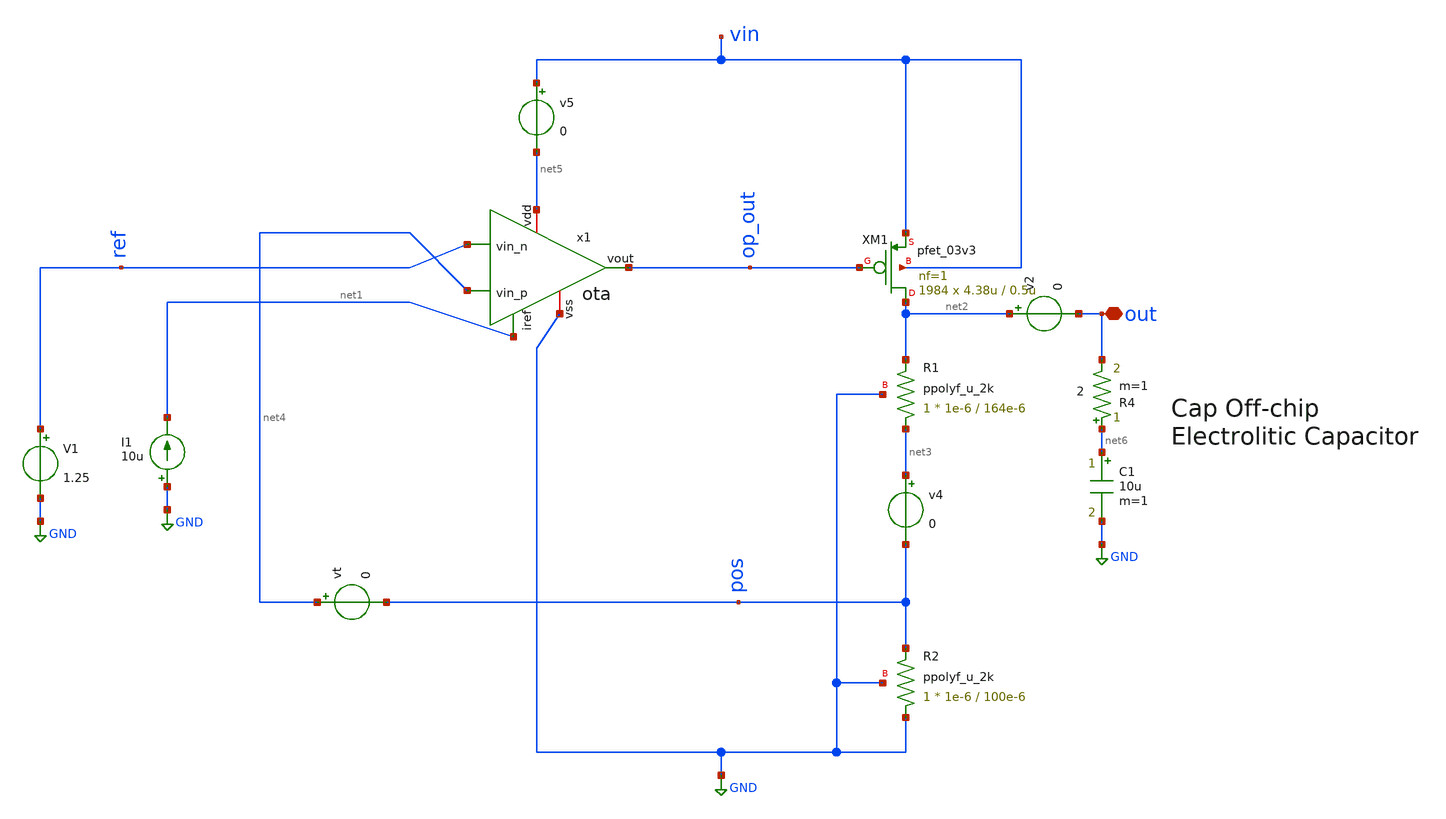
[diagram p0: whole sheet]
** sch_path: LDO/xschem/ldo/test/load_regulation.sch

.include $env(PDK_ROOT)/$env(PDK)/libs.tech/ngspice/design.ngspice
.lib $env(PDK_ROOT)/$env(PDK)/libs.tech/ngspice/sm141064.ngspice typical
.lib $env(PDK_ROOT)/$env(PDK)/libs.tech/ngspice/sm141064.ngspice res_typical

.lib $env(PDK_ROOT)/$env(PDK)/libs.tech/ngspice/sm141064.ngspice cap_mim
.lib $env(PDK_ROOT)/$env(PDK)/libs.tech/ngspice/sm141064.ngspice mimcap_typical


**.subckt load_regulation out
*.iopin out
I1 GND net1 10u
V1 ref GND 1.25
XM1 net2 op_out vin vin pfet_03v3 L=0.5u W=4.38u nf=1 ad='int((nf+1)/2) * W/nf * 0.18u' as='int((nf+2)/2) * W/nf * 0.18u'
+ pd='2*int((nf+1)/2) * (W/nf + 0.18u)' ps='2*int((nf+2)/2) * (W/nf + 0.18u)' nrd='0.18u / W' nrs='0.18u / W'
+ sa=0 sb=0 sd=0 m=1984
XR1 net3 net2 GND ppolyf_u_2k r_width=1e-6 r_length=164e-6 m=1
XR2 GND pos GND ppolyf_u_2k r_width=1e-6 r_length=100e-6 m=1
v4 net3 pos 0
vt net4 pos 0
v2 net2 out 0
v5 vin net5 0
x1 net5 net1 ref net4 op_out GND ota
C1 net6 GND 10u m=1
R4 net6 out 2 m=1
**** begin user architecture code


.param R=33
R10 out 0 {R}
IL out 0 PWL(0 0.1m 10u 0.1m 20u 10m 30u 10m)

.param iref = 10u
.param vdd  = 5
.param vss  = 0.0
.param vcm  = 1.25
.param vac  = 60m
.param w857 = 5u
.param l857 = 1u
.param m857 = 1
.param wpar = 10u
.param lpar = 1u
.param mpar = 1
.param w34  = 10u
.param l34  = 1u
.param m34  = 1
.param w6   = 100u
.param l6   = 1u
.param m6   = 1

.param m5   = 1
.param m7   = 5


Vs vin 0 5

.nodeset v(out)=0
.nodeset v(x1.pos)=0

**Load_Transient
.control
reset
alter IL 50u
alter R10 3600k
tran 0.1u 100u
meas TRAN V_ldo_100u FIND v(out) AT=5u
meas TRAN V_ldo_10m FIND v(out) AT=100u
let load_reg= V_ldo_100u-V_ldo_10m
let load_current =(-1*i(Vs)-131.8e-6)
print load_reg/9.9
plot i(v2) v(out)-3.3
.endc


**** end user architecture code
**.ends
.GLOBAL GND
.end
